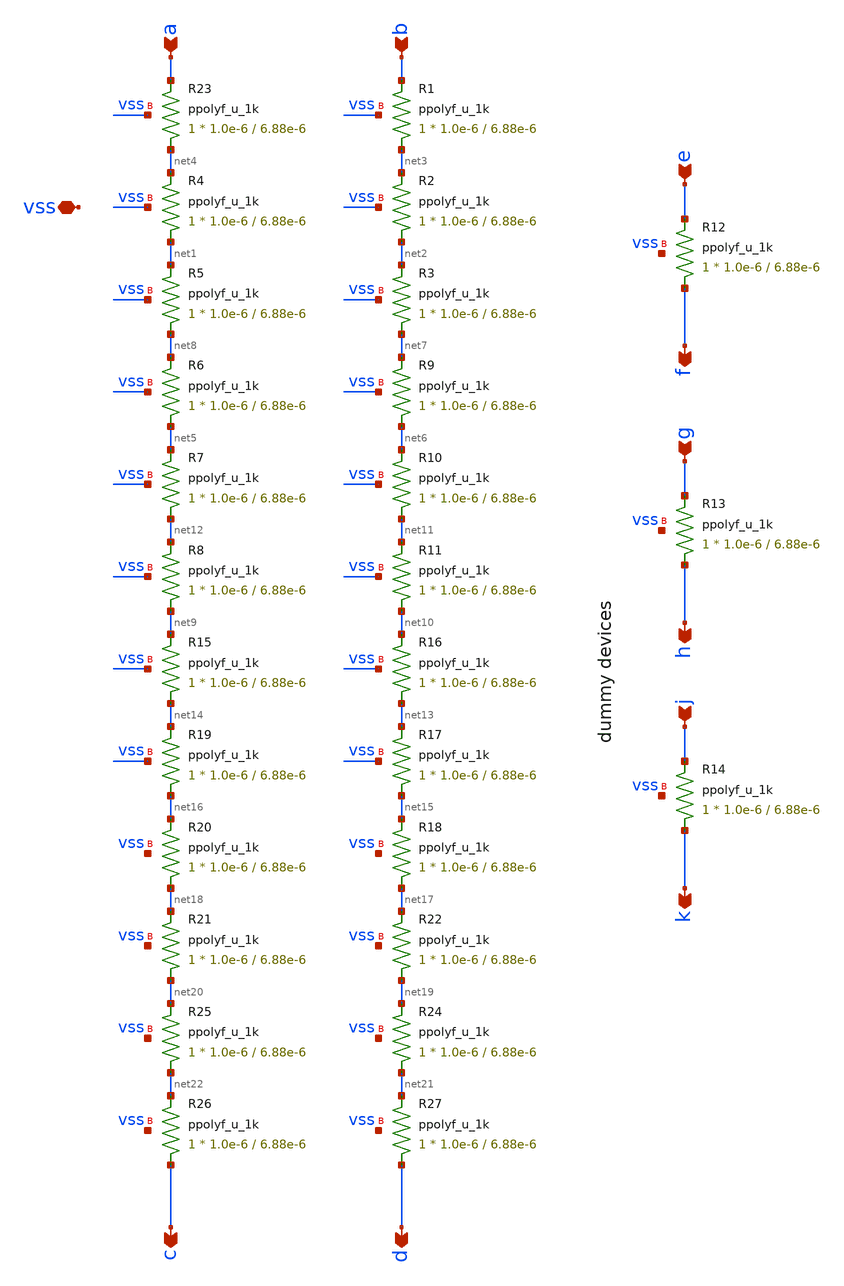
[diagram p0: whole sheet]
** sch_path: xschem/bg_res.sch
**.subckt bg_res a b c d vss f e h g k j
*.ipin a
*.ipin b
*.opin c
*.opin d
*.iopin vss
*.opin f
*.ipin e
*.opin h
*.ipin g
*.opin k
*.ipin j
XR23 net4 a vss ppolyf_u_1k r_width=1.0e-6 r_length=6.88e-6 m=1
XR1 net3 b vss ppolyf_u_1k r_width=1.0e-6 r_length=6.88e-6 m=1
XR2 net2 net3 vss ppolyf_u_1k r_width=1.0e-6 r_length=6.88e-6 m=1
XR3 net7 net2 vss ppolyf_u_1k r_width=1.0e-6 r_length=6.88e-6 m=1
XR4 net1 net4 vss ppolyf_u_1k r_width=1.0e-6 r_length=6.88e-6 m=1
XR5 net8 net1 vss ppolyf_u_1k r_width=1.0e-6 r_length=6.88e-6 m=1
XR6 net5 net8 vss ppolyf_u_1k r_width=1.0e-6 r_length=6.88e-6 m=1
XR7 net12 net5 vss ppolyf_u_1k r_width=1.0e-6 r_length=6.88e-6 m=1
XR8 net9 net12 vss ppolyf_u_1k r_width=1.0e-6 r_length=6.88e-6 m=1
XR9 net6 net7 vss ppolyf_u_1k r_width=1.0e-6 r_length=6.88e-6 m=1
XR10 net11 net6 vss ppolyf_u_1k r_width=1.0e-6 r_length=6.88e-6 m=1
XR11 net10 net11 vss ppolyf_u_1k r_width=1.0e-6 r_length=6.88e-6 m=1
XR12 f e vss ppolyf_u_1k r_width=1.0e-6 r_length=6.88e-6 m=1
XR13 h g vss ppolyf_u_1k r_width=1.0e-6 r_length=6.88e-6 m=1
XR14 k j vss ppolyf_u_1k r_width=1.0e-6 r_length=6.88e-6 m=1
XR15 net14 net9 vss ppolyf_u_1k r_width=1.0e-6 r_length=6.88e-6 m=1
XR16 net13 net10 vss ppolyf_u_1k r_width=1.0e-6 r_length=6.88e-6 m=1
XR17 net15 net13 vss ppolyf_u_1k r_width=1.0e-6 r_length=6.88e-6 m=1
XR18 net17 net15 vss ppolyf_u_1k r_width=1.0e-6 r_length=6.88e-6 m=1
XR19 net16 net14 vss ppolyf_u_1k r_width=1.0e-6 r_length=6.88e-6 m=1
XR20 net18 net16 vss ppolyf_u_1k r_width=1.0e-6 r_length=6.88e-6 m=1
XR21 net20 net18 vss ppolyf_u_1k r_width=1.0e-6 r_length=6.88e-6 m=1
XR22 net19 net17 vss ppolyf_u_1k r_width=1.0e-6 r_length=6.88e-6 m=1
XR24 net21 net19 vss ppolyf_u_1k r_width=1.0e-6 r_length=6.88e-6 m=1
XR25 net22 net20 vss ppolyf_u_1k r_width=1.0e-6 r_length=6.88e-6 m=1
XR26 c net22 vss ppolyf_u_1k r_width=1.0e-6 r_length=6.88e-6 m=1
XR27 d net21 vss ppolyf_u_1k r_width=1.0e-6 r_length=6.88e-6 m=1
**.ends
.end
